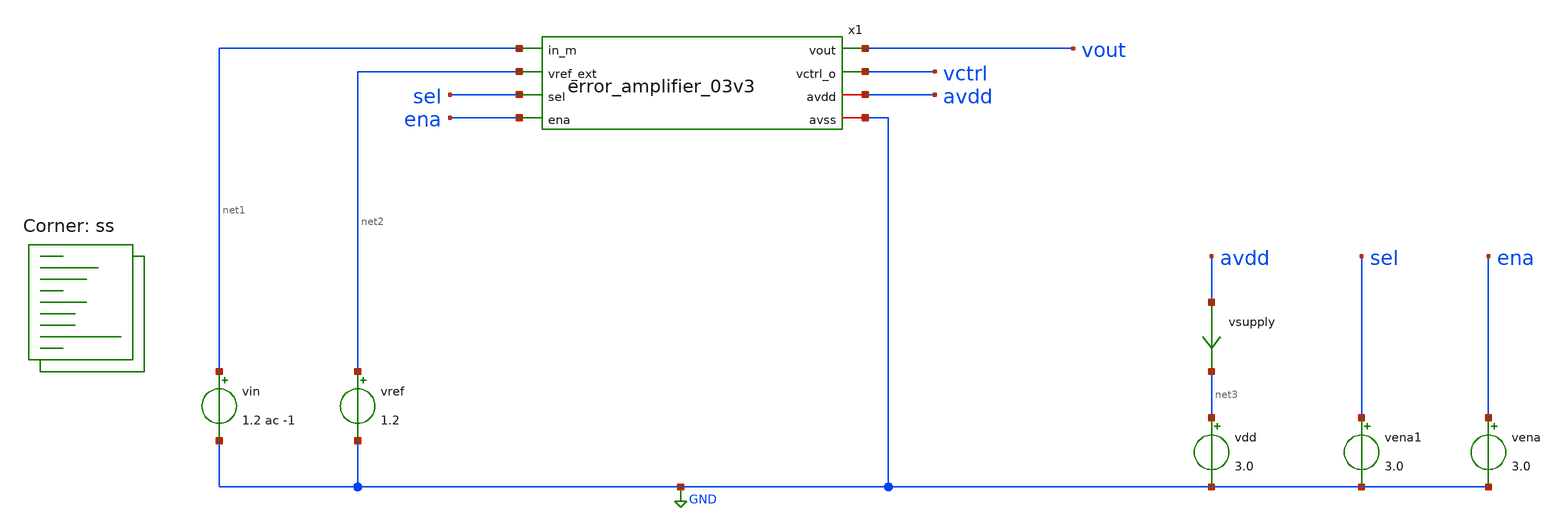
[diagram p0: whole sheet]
** sch_path: xschem/error_amplifier_03v3_tb.sch
**.subckt error_amplifier_03v3_tb
vdd net3 GND 3.0
vsupply avdd net3 0
.save i(vsupply)
vena ena GND 3.0
x1 vout net1 vctrl net2 sel ena avdd GND error_amplifier_03v3
vref net2 GND 1.2
vin net1 GND 1.2 ac -1
vena1 sel GND 3.0
**** begin user architecture code

* ngspice control
.option savecurrents
.control
save all
save @m.x1.xm26.msky130_fd_pr__pfet_g5v0d10v5[gds]
save @m.x1.xm28.msky130_fd_pr__pfet_g5v0d10v5[gm]
save @m.x1.xm28.msky130_fd_pr__pfet_g5v0d10v5[gds]
save @m.x1.xm30.msky130_fd_pr__nfet_g5v0d10v5[gm]
save @m.x1.xm30.msky130_fd_pr__nfet_g5v0d10v5[gds]
save @m.x1.xm32.msky130_fd_pr__nfet_g5v0d10v5[gds]
save @m.x1.xm6.msky130_fd_pr__nfet_g5v0d10v5[gds]

save @m.x1.xm9.msky130_fd_pr__pfet_g5v0d10v5[gm]
save @m.x1.xm9.msky130_fd_pr__pfet_g5v0d10v5[gds]
save @m.x1.xm9.msky130_fd_pr__pfet_g5v0d10v5[gmbs]
save @m.x1.xm39.msky130_fd_pr__nfet_g5v0d10v5[gm]
save @m.x1.xm8.msky130_fd_pr__pfet_g5v0d10v5[gds]
save @m.x1.xm38.msky130_fd_pr__nfet_g5v0d10v5[gds]
op
write error_amplifier_03v3_tb.raw
set appendwrite

let av28 = @m.x1.xm28.msky130_fd_pr__pfet_g5v0d10v5[gm] /
+ @m.x1.xm28.msky130_fd_pr__pfet_g5v0d10v5[gds]
let av30 = @m.x1.xm30.msky130_fd_pr__nfet_g5v0d10v5[gm] /
+ @m.x1.xm30.msky130_fd_pr__nfet_g5v0d10v5[gds]

echo pfet
print @m.x1.xm26.msky130_fd_pr__pfet_g5v0d10v5[gds]
print @m.x1.xm6.msky130_fd_pr__nfet_g5v0d10v5[gds]
print av28

echo nfet
print @m.x1.xm32.msky130_fd_pr__nfet_g5v0d10v5[gds]
print av30

echo 'super source follower'
print @m.x1.xm9.msky130_fd_pr__pfet_g5v0d10v5[gm]
print @m.x1.xm9.msky130_fd_pr__pfet_g5v0d10v5[gds]
print @m.x1.xm9.msky130_fd_pr__pfet_g5v0d10v5[gmbs]
print @m.x1.xm39.msky130_fd_pr__nfet_g5v0d10v5[gm]
print @m.x1.xm8.msky130_fd_pr__pfet_g5v0d10v5[gds]
print @m.x1.xm38.msky130_fd_pr__nfet_g5v0d10v5[gds]

optran 0 0 0 1u 20u 0

ac dec 10 10 10e6
set units=degrees
plot db(vctrl)
plot ph(vctrl)

let gain = db(vctrl)
let ph = ph(vctrl)
meas ac p1 when ph = -45
meas ac p2 when ph = -135
meas ac s_gain find gain at=10
meas ac ph_margin find ph when gain = 1
print ph_margin + 180

dc vref 1.18 1.21 100u
plot vctrl

*tran 1u 20u
*plot vout x1.vbp x1.vcp x1.vcn x1.vbn
.endc


.lib $::SKYWATER_MODELS/sky130.lib.spice ss
**** end user architecture code
**.ends

* expanding   symbol:  error_amplifier_03v3.sym # of pins=8
** sym_path: xschem/error_amplifier_03v3.sym
** sch_path: xschem/error_amplifier_03v3.sch
.subckt error_amplifier_03v3 vout in_m vctrl_o vref_ext sel ena avdd avss
*.ipin in_m
*.ipin ena
*.iopin avdd
*.iopin avss
*.opin vout
*.opin vctrl_o
*.ipin sel
*.ipin vref_ext
XM1 vbn vbn avss avss sky130_fd_pr__nfet_g5v0d10v5 L=10 W=1 nf=1 ad='int((nf+1)/2) * W/nf * 0.29' as='int((nf+2)/2) * W/nf * 0.29'
+ pd='2*int((nf+1)/2) * (W/nf + 0.29)' ps='2*int((nf+2)/2) * (W/nf + 0.29)' nrd='0.29 / W' nrs='0.29 / W'
+ sa=0 sb=0 sd=0 mult=1 m=1
XM3 vcp vbn net5 avss sky130_fd_pr__nfet_g5v0d10v5 L=10 W=1 nf=1 ad='int((nf+1)/2) * W/nf * 0.29' as='int((nf+2)/2) * W/nf * 0.29'
+ pd='2*int((nf+1)/2) * (W/nf + 0.29)' ps='2*int((nf+2)/2) * (W/nf + 0.29)' nrd='0.29 / W' nrs='0.29 / W'
+ sa=0 sb=0 sd=0 mult=4 m=4
XM5 vbp vbp avdd avdd sky130_fd_pr__pfet_g5v0d10v5 L=10 W=1 nf=1 ad='int((nf+1)/2) * W/nf * 0.29' as='int((nf+2)/2) * W/nf * 0.29'
+ pd='2*int((nf+1)/2) * (W/nf + 0.29)' ps='2*int((nf+2)/2) * (W/nf + 0.29)' nrd='0.29 / W' nrs='0.29 / W'
+ sa=0 sb=0 sd=0 mult=2 m=2
XM26 net3 vbp avdd avdd sky130_fd_pr__pfet_g5v0d10v5 L=10 W=1 nf=1 ad='int((nf+1)/2) * W/nf * 0.29' as='int((nf+2)/2) * W/nf * 0.29'
+ pd='2*int((nf+1)/2) * (W/nf + 0.29)' ps='2*int((nf+2)/2) * (W/nf + 0.29)' nrd='0.29 / W' nrs='0.29 / W'
+ sa=0 sb=0 sd=0 mult=6 m=6
XM27 net4 vbp avdd avdd sky130_fd_pr__pfet_g5v0d10v5 L=10 W=1 nf=1 ad='int((nf+1)/2) * W/nf * 0.29' as='int((nf+2)/2) * W/nf * 0.29'
+ pd='2*int((nf+1)/2) * (W/nf + 0.29)' ps='2*int((nf+2)/2) * (W/nf + 0.29)' nrd='0.29 / W' nrs='0.29 / W'
+ sa=0 sb=0 sd=0 mult=6 m=6
XM28 vx vcp net3 avdd sky130_fd_pr__pfet_g5v0d10v5 L=1 W=1 nf=1 ad='int((nf+1)/2) * W/nf * 0.29' as='int((nf+2)/2) * W/nf * 0.29'
+ pd='2*int((nf+1)/2) * (W/nf + 0.29)' ps='2*int((nf+2)/2) * (W/nf + 0.29)' nrd='0.29 / W' nrs='0.29 / W'
+ sa=0 sb=0 sd=0 mult=1 m=1
XM29 v_cascode vcp net4 avdd sky130_fd_pr__pfet_g5v0d10v5 L=1 W=1 nf=1 ad='int((nf+1)/2) * W/nf * 0.29'
+ as='int((nf+2)/2) * W/nf * 0.29' pd='2*int((nf+1)/2) * (W/nf + 0.29)' ps='2*int((nf+2)/2) * (W/nf + 0.29)'
+ nrd='0.29 / W' nrs='0.29 / W' sa=0 sb=0 sd=0 mult=1 m=1
XM30 vx vcn net1 avss sky130_fd_pr__nfet_g5v0d10v5 L=1 W=1 nf=1 ad='int((nf+1)/2) * W/nf * 0.29' as='int((nf+2)/2) * W/nf * 0.29'
+ pd='2*int((nf+1)/2) * (W/nf + 0.29)' ps='2*int((nf+2)/2) * (W/nf + 0.29)' nrd='0.29 / W' nrs='0.29 / W'
+ sa=0 sb=0 sd=0 mult=1 m=1
XM31 v_cascode vcn net2 avss sky130_fd_pr__nfet_g5v0d10v5 L=1 W=1 nf=1 ad='int((nf+1)/2) * W/nf * 0.29'
+ as='int((nf+2)/2) * W/nf * 0.29' pd='2*int((nf+1)/2) * (W/nf + 0.29)' ps='2*int((nf+2)/2) * (W/nf + 0.29)'
+ nrd='0.29 / W' nrs='0.29 / W' sa=0 sb=0 sd=0 mult=1 m=1
XM32 net1 vx avss avss sky130_fd_pr__nfet_g5v0d10v5 L=2 W=1 nf=1 ad='int((nf+1)/2) * W/nf * 0.29' as='int((nf+2)/2) * W/nf * 0.29'
+ pd='2*int((nf+1)/2) * (W/nf + 0.29)' ps='2*int((nf+2)/2) * (W/nf + 0.29)' nrd='0.29 / W' nrs='0.29 / W'
+ sa=0 sb=0 sd=0 mult=1 m=1
XM33 net2 vx avss avss sky130_fd_pr__nfet_g5v0d10v5 L=2 W=1 nf=1 ad='int((nf+1)/2) * W/nf * 0.29' as='int((nf+2)/2) * W/nf * 0.29'
+ pd='2*int((nf+1)/2) * (W/nf + 0.29)' ps='2*int((nf+2)/2) * (W/nf + 0.29)' nrd='0.29 / W' nrs='0.29 / W'
+ sa=0 sb=0 sd=0 mult=1 m=1
XM35 net10 vbp avdd avdd sky130_fd_pr__pfet_g5v0d10v5 L=10 W=1 nf=1 ad='int((nf+1)/2) * W/nf * 0.29'
+ as='int((nf+2)/2) * W/nf * 0.29' pd='2*int((nf+1)/2) * (W/nf + 0.29)' ps='2*int((nf+2)/2) * (W/nf + 0.29)'
+ nrd='0.29 / W' nrs='0.29 / W' sa=0 sb=0 sd=0 mult=2 m=2
XR3 avss net5 avss sky130_fd_pr__res_xhigh_po_0p35 L=180 mult=1 m=1
XM9 net11 v_cascode v_ea avdd sky130_fd_pr__pfet_g5v0d10v5 L=0.5 W=1 nf=1 ad='int((nf+1)/2) * W/nf * 0.29'
+ as='int((nf+2)/2) * W/nf * 0.29' pd='2*int((nf+1)/2) * (W/nf + 0.29)' ps='2*int((nf+2)/2) * (W/nf + 0.29)'
+ nrd='0.29 / W' nrs='0.29 / W' sa=0 sb=0 sd=0 mult=1 m=1
XM8 v_ea vbp avdd avdd sky130_fd_pr__pfet_g5v0d10v5 L=10 W=1 nf=1 ad='int((nf+1)/2) * W/nf * 0.29' as='int((nf+2)/2) * W/nf * 0.29'
+ pd='2*int((nf+1)/2) * (W/nf + 0.29)' ps='2*int((nf+2)/2) * (W/nf + 0.29)' nrd='0.29 / W' nrs='0.29 / W'
+ sa=0 sb=0 sd=0 mult=10 m=10
XM17 net7 vbp avdd avdd sky130_fd_pr__pfet_g5v0d10v5 L=10 W=1 nf=1 ad='int((nf+1)/2) * W/nf * 0.29' as='int((nf+2)/2) * W/nf * 0.29'
+ pd='2*int((nf+1)/2) * (W/nf + 0.29)' ps='2*int((nf+2)/2) * (W/nf + 0.29)' nrd='0.29 / W' nrs='0.29 / W'
+ sa=0 sb=0 sd=0 mult=1 m=1
XM19 net7 net7 net6 avss sky130_fd_pr__nfet_g5v0d10v5 L=0.5 W=1 nf=1 ad='int((nf+1)/2) * W/nf * 0.29'
+ as='int((nf+2)/2) * W/nf * 0.29' pd='2*int((nf+1)/2) * (W/nf + 0.29)' ps='2*int((nf+2)/2) * (W/nf + 0.29)'
+ nrd='0.29 / W' nrs='0.29 / W' sa=0 sb=0 sd=0 mult=6 m=6
XM20 net6 net7 avss avss sky130_fd_pr__nfet_g5v0d10v5 L=0.5 W=1 nf=1 ad='int((nf+1)/2) * W/nf * 0.29'
+ as='int((nf+2)/2) * W/nf * 0.29' pd='2*int((nf+1)/2) * (W/nf + 0.29)' ps='2*int((nf+2)/2) * (W/nf + 0.29)'
+ nrd='0.29 / W' nrs='0.29 / W' sa=0 sb=0 sd=0 mult=1 m=1
XM21 vcn vbp avdd avdd sky130_fd_pr__pfet_g5v0d10v5 L=10 W=1 nf=1 ad='int((nf+1)/2) * W/nf * 0.29' as='int((nf+2)/2) * W/nf * 0.29'
+ pd='2*int((nf+1)/2) * (W/nf + 0.29)' ps='2*int((nf+2)/2) * (W/nf + 0.29)' nrd='0.29 / W' nrs='0.29 / W'
+ sa=0 sb=0 sd=0 mult=5 m=5
XM36 vcn vcn net6 avss sky130_fd_pr__nfet_g5v0d10v5 L=2 W=1 nf=1 ad='int((nf+1)/2) * W/nf * 0.29' as='int((nf+2)/2) * W/nf * 0.29'
+ pd='2*int((nf+1)/2) * (W/nf + 0.29)' ps='2*int((nf+2)/2) * (W/nf + 0.29)' nrd='0.29 / W' nrs='0.29 / W'
+ sa=0 sb=0 sd=0 mult=1 m=1
XM6 net4 in_m net8 avss sky130_fd_pr__nfet_g5v0d10v5 L=0.5 W=1 nf=1 ad='int((nf+1)/2) * W/nf * 0.29'
+ as='int((nf+2)/2) * W/nf * 0.29' pd='2*int((nf+1)/2) * (W/nf + 0.29)' ps='2*int((nf+2)/2) * (W/nf + 0.29)'
+ nrd='0.29 / W' nrs='0.29 / W' sa=0 sb=0 sd=0 mult=1 m=1
XM7 net8 vbn avss avss sky130_fd_pr__nfet_g5v0d10v5 L=10 W=1 nf=1 ad='int((nf+1)/2) * W/nf * 0.29' as='int((nf+2)/2) * W/nf * 0.29'
+ pd='2*int((nf+1)/2) * (W/nf + 0.29)' ps='2*int((nf+2)/2) * (W/nf + 0.29)' nrd='0.29 / W' nrs='0.29 / W'
+ sa=0 sb=0 sd=0 mult=2 m=2
XM12 net3 in_p net8 avss sky130_fd_pr__nfet_g5v0d10v5 L=0.5 W=1 nf=1 ad='int((nf+1)/2) * W/nf * 0.29'
+ as='int((nf+2)/2) * W/nf * 0.29' pd='2*int((nf+1)/2) * (W/nf + 0.29)' ps='2*int((nf+2)/2) * (W/nf + 0.29)'
+ nrd='0.29 / W' nrs='0.29 / W' sa=0 sb=0 sd=0 mult=1 m=1
XM10 vstart vbn avss avss sky130_fd_pr__nfet_g5v0d10v5 L=1 W=10 nf=1 ad='int((nf+1)/2) * W/nf * 0.29'
+ as='int((nf+2)/2) * W/nf * 0.29' pd='2*int((nf+1)/2) * (W/nf + 0.29)' ps='2*int((nf+2)/2) * (W/nf + 0.29)'
+ nrd='0.29 / W' nrs='0.29 / W' sa=0 sb=0 sd=0 mult=1 m=1
XM11 vstart ena_b net9 avdd sky130_fd_pr__pfet_g5v0d10v5 L=20 W=1 nf=1 ad='int((nf+1)/2) * W/nf * 0.29'
+ as='int((nf+2)/2) * W/nf * 0.29' pd='2*int((nf+1)/2) * (W/nf + 0.29)' ps='2*int((nf+2)/2) * (W/nf + 0.29)'
+ nrd='0.29 / W' nrs='0.29 / W' sa=0 sb=0 sd=0 mult=1 m=1
XM2 vcp vcp vbp avdd sky130_fd_pr__pfet_g5v0d10v5 L=4 W=1 nf=1 ad='int((nf+1)/2) * W/nf * 0.29' as='int((nf+2)/2) * W/nf * 0.29'
+ pd='2*int((nf+1)/2) * (W/nf + 0.29)' ps='2*int((nf+2)/2) * (W/nf + 0.29)' nrd='0.29 / W' nrs='0.29 / W'
+ sa=0 sb=0 sd=0 mult=1 m=1
XM4 vbn vcp net10 avdd sky130_fd_pr__pfet_g5v0d10v5 L=4 W=1 nf=1 ad='int((nf+1)/2) * W/nf * 0.29' as='int((nf+2)/2) * W/nf * 0.29'
+ pd='2*int((nf+1)/2) * (W/nf + 0.29)' ps='2*int((nf+2)/2) * (W/nf + 0.29)' nrd='0.29 / W' nrs='0.29 / W'
+ sa=0 sb=0 sd=0 mult=1 m=1
XM13 vbp vstart avss avss sky130_fd_pr__nfet_g5v0d10v5 L=0.5 W=1 nf=1 ad='int((nf+1)/2) * W/nf * 0.29'
+ as='int((nf+2)/2) * W/nf * 0.29' pd='2*int((nf+1)/2) * (W/nf + 0.29)' ps='2*int((nf+2)/2) * (W/nf + 0.29)'
+ nrd='0.29 / W' nrs='0.29 / W' sa=0 sb=0 sd=0 mult=1 m=1
XM14 vcp vstart avss avss sky130_fd_pr__nfet_g5v0d10v5 L=0.5 W=1 nf=1 ad='int((nf+1)/2) * W/nf * 0.29'
+ as='int((nf+2)/2) * W/nf * 0.29' pd='2*int((nf+1)/2) * (W/nf + 0.29)' ps='2*int((nf+2)/2) * (W/nf + 0.29)'
+ nrd='0.29 / W' nrs='0.29 / W' sa=0 sb=0 sd=0 mult=1 m=1
XM15 net9 net9 avdd avdd sky130_fd_pr__pfet_g5v0d10v5 L=20 W=1 nf=1 ad='int((nf+1)/2) * W/nf * 0.29'
+ as='int((nf+2)/2) * W/nf * 0.29' pd='2*int((nf+1)/2) * (W/nf + 0.29)' ps='2*int((nf+2)/2) * (W/nf + 0.29)'
+ nrd='0.29 / W' nrs='0.29 / W' sa=0 sb=0 sd=0 mult=1 m=1
XM16 vbp ena avdd avdd sky130_fd_pr__pfet_g5v0d10v5 L=0.5 W=1 nf=1 ad='int((nf+1)/2) * W/nf * 0.29' as='int((nf+2)/2) * W/nf * 0.29'
+ pd='2*int((nf+1)/2) * (W/nf + 0.29)' ps='2*int((nf+2)/2) * (W/nf + 0.29)' nrd='0.29 / W' nrs='0.29 / W'
+ sa=0 sb=0 sd=0 mult=1 m=1
XM18 vcp ena avdd avdd sky130_fd_pr__pfet_g5v0d10v5 L=0.5 W=1 nf=1 ad='int((nf+1)/2) * W/nf * 0.29' as='int((nf+2)/2) * W/nf * 0.29'
+ pd='2*int((nf+1)/2) * (W/nf + 0.29)' ps='2*int((nf+2)/2) * (W/nf + 0.29)' nrd='0.29 / W' nrs='0.29 / W'
+ sa=0 sb=0 sd=0 mult=1 m=1
XM22 vbn ena_b avss avss sky130_fd_pr__nfet_g5v0d10v5 L=0.5 W=1 nf=1 ad='int((nf+1)/2) * W/nf * 0.29'
+ as='int((nf+2)/2) * W/nf * 0.29' pd='2*int((nf+1)/2) * (W/nf + 0.29)' ps='2*int((nf+2)/2) * (W/nf + 0.29)'
+ nrd='0.29 / W' nrs='0.29 / W' sa=0 sb=0 sd=0 mult=1 m=1
XM23 vcn ena_b avss avss sky130_fd_pr__nfet_g5v0d10v5 L=0.5 W=1 nf=1 ad='int((nf+1)/2) * W/nf * 0.29'
+ as='int((nf+2)/2) * W/nf * 0.29' pd='2*int((nf+1)/2) * (W/nf + 0.29)' ps='2*int((nf+2)/2) * (W/nf + 0.29)'
+ nrd='0.29 / W' nrs='0.29 / W' sa=0 sb=0 sd=0 mult=1 m=1
XM24 v_cascode ena_b avss avss sky130_fd_pr__nfet_g5v0d10v5 L=0.5 W=1 nf=1 ad='int((nf+1)/2) * W/nf * 0.29'
+ as='int((nf+2)/2) * W/nf * 0.29' pd='2*int((nf+1)/2) * (W/nf + 0.29)' ps='2*int((nf+2)/2) * (W/nf + 0.29)'
+ nrd='0.29 / W' nrs='0.29 / W' sa=0 sb=0 sd=0 mult=1 m=1
XM25 v_ea ena_b avss avss sky130_fd_pr__nfet_g5v0d10v5 L=0.5 W=1 nf=1 ad='int((nf+1)/2) * W/nf * 0.29'
+ as='int((nf+2)/2) * W/nf * 0.29' pd='2*int((nf+1)/2) * (W/nf + 0.29)' ps='2*int((nf+2)/2) * (W/nf + 0.29)'
+ nrd='0.29 / W' nrs='0.29 / W' sa=0 sb=0 sd=0 mult=1 m=1
XM34 vstart ena_b avss avss sky130_fd_pr__nfet_g5v0d10v5 L=0.5 W=1 nf=1 ad='int((nf+1)/2) * W/nf * 0.29'
+ as='int((nf+2)/2) * W/nf * 0.29' pd='2*int((nf+1)/2) * (W/nf + 0.29)' ps='2*int((nf+2)/2) * (W/nf + 0.29)'
+ nrd='0.29 / W' nrs='0.29 / W' sa=0 sb=0 sd=0 mult=1 m=1
XM38 net11 vbn avss avss sky130_fd_pr__nfet_g5v0d10v5 L=10 W=1 nf=1 ad='int((nf+1)/2) * W/nf * 0.29'
+ as='int((nf+2)/2) * W/nf * 0.29' pd='2*int((nf+1)/2) * (W/nf + 0.29)' ps='2*int((nf+2)/2) * (W/nf + 0.29)'
+ nrd='0.29 / W' nrs='0.29 / W' sa=0 sb=0 sd=0 mult=2 m=2
XM39 v_ea net11 avss avss sky130_fd_pr__nfet_g5v0d10v5 L=0.5 W=1 nf=1 ad='int((nf+1)/2) * W/nf * 0.29'
+ as='int((nf+2)/2) * W/nf * 0.29' pd='2*int((nf+1)/2) * (W/nf + 0.29)' ps='2*int((nf+2)/2) * (W/nf + 0.29)'
+ nrd='0.29 / W' nrs='0.29 / W' sa=0 sb=0 sd=0 mult=1 m=1
XM40 vref_int vbp avdd avdd sky130_fd_pr__pfet_g5v0d10v5 L=10 W=1 nf=1 ad='int((nf+1)/2) * W/nf * 0.29'
+ as='int((nf+2)/2) * W/nf * 0.29' pd='2*int((nf+1)/2) * (W/nf + 0.29)' ps='2*int((nf+2)/2) * (W/nf + 0.29)'
+ nrd='0.29 / W' nrs='0.29 / W' sa=0 sb=0 sd=0 mult=15 m=15
XM47 vref_int vref_int avss avss sky130_fd_pr__nfet_g5v0d10v5 L=20 W=1.05 nf=1 ad='int((nf+1)/2) * W/nf * 0.29'
+ as='int((nf+2)/2) * W/nf * 0.29' pd='2*int((nf+1)/2) * (W/nf + 0.29)' ps='2*int((nf+2)/2) * (W/nf + 0.29)'
+ nrd='0.29 / W' nrs='0.29 / W' sa=0 sb=0 sd=0 mult=1 m=1
XM37 ena_b ena avdd avdd sky130_fd_pr__pfet_g5v0d10v5 L=0.5 W=3.5 nf=1 ad='int((nf+1)/2) * W/nf * 0.29'
+ as='int((nf+2)/2) * W/nf * 0.29' pd='2*int((nf+1)/2) * (W/nf + 0.29)' ps='2*int((nf+2)/2) * (W/nf + 0.29)'
+ nrd='0.29 / W' nrs='0.29 / W' sa=0 sb=0 sd=0 mult=1 m=1
XM41 ena_b ena avss avss sky130_fd_pr__nfet_g5v0d10v5 L=0.5 W=1 nf=1 ad='int((nf+1)/2) * W/nf * 0.29'
+ as='int((nf+2)/2) * W/nf * 0.29' pd='2*int((nf+1)/2) * (W/nf + 0.29)' ps='2*int((nf+2)/2) * (W/nf + 0.29)'
+ nrd='0.29 / W' nrs='0.29 / W' sa=0 sb=0 sd=0 mult=1 m=1
XC2 v_cascode avss sky130_fd_pr__cap_mim_m3_1 W=3.5 L=3.5 MF=1 m=1
XR1 vctrl_o vout avss sky130_fd_pr__res_xhigh_po_0p35 L=180 mult=1 m=1
XR2 avss vctrl_o avss sky130_fd_pr__res_xhigh_po_0p35 L=360 mult=1 m=1
XM42 avdd v_ea vout avss sky130_fd_pr__nfet_g5v0d10v5 L=0.5 W=200 nf=1 ad='int((nf+1)/2) * W/nf * 0.29'
+ as='int((nf+2)/2) * W/nf * 0.29' pd='2*int((nf+1)/2) * (W/nf + 0.29)' ps='2*int((nf+2)/2) * (W/nf + 0.29)'
+ nrd='0.29 / W' nrs='0.29 / W' sa=0 sb=0 sd=0 mult=1 m=1
XM43 in_p sel vref_int avdd sky130_fd_pr__pfet_g5v0d10v5 L=0.5 W=1 nf=1 ad='int((nf+1)/2) * W/nf * 0.29'
+ as='int((nf+2)/2) * W/nf * 0.29' pd='2*int((nf+1)/2) * (W/nf + 0.29)' ps='2*int((nf+2)/2) * (W/nf + 0.29)'
+ nrd='0.29 / W' nrs='0.29 / W' sa=0 sb=0 sd=0 mult=1 m=1
XM49 vref_int sel_b in_p avss sky130_fd_pr__nfet_g5v0d10v5 L=0.5 W=1 nf=1 ad='int((nf+1)/2) * W/nf * 0.29'
+ as='int((nf+2)/2) * W/nf * 0.29' pd='2*int((nf+1)/2) * (W/nf + 0.29)' ps='2*int((nf+2)/2) * (W/nf + 0.29)'
+ nrd='0.29 / W' nrs='0.29 / W' sa=0 sb=0 sd=0 mult=1 m=1
XM50 in_p sel_b vref_ext avdd sky130_fd_pr__pfet_g5v0d10v5 L=0.5 W=1 nf=1 ad='int((nf+1)/2) * W/nf * 0.29'
+ as='int((nf+2)/2) * W/nf * 0.29' pd='2*int((nf+1)/2) * (W/nf + 0.29)' ps='2*int((nf+2)/2) * (W/nf + 0.29)'
+ nrd='0.29 / W' nrs='0.29 / W' sa=0 sb=0 sd=0 mult=1 m=1
XM51 vref_ext sel in_p avss sky130_fd_pr__nfet_g5v0d10v5 L=0.5 W=1 nf=1 ad='int((nf+1)/2) * W/nf * 0.29'
+ as='int((nf+2)/2) * W/nf * 0.29' pd='2*int((nf+1)/2) * (W/nf + 0.29)' ps='2*int((nf+2)/2) * (W/nf + 0.29)'
+ nrd='0.29 / W' nrs='0.29 / W' sa=0 sb=0 sd=0 mult=1 m=1
XM44 sel_b sel avdd avdd sky130_fd_pr__pfet_g5v0d10v5 L=0.5 W=3.5 nf=1 ad='int((nf+1)/2) * W/nf * 0.29'
+ as='int((nf+2)/2) * W/nf * 0.29' pd='2*int((nf+1)/2) * (W/nf + 0.29)' ps='2*int((nf+2)/2) * (W/nf + 0.29)'
+ nrd='0.29 / W' nrs='0.29 / W' sa=0 sb=0 sd=0 mult=1 m=1
XM45 sel_b sel avss avss sky130_fd_pr__nfet_g5v0d10v5 L=0.5 W=1 nf=1 ad='int((nf+1)/2) * W/nf * 0.29'
+ as='int((nf+2)/2) * W/nf * 0.29' pd='2*int((nf+1)/2) * (W/nf + 0.29)' ps='2*int((nf+2)/2) * (W/nf + 0.29)'
+ nrd='0.29 / W' nrs='0.29 / W' sa=0 sb=0 sd=0 mult=1 m=1
.ends

.GLOBAL GND
.end
